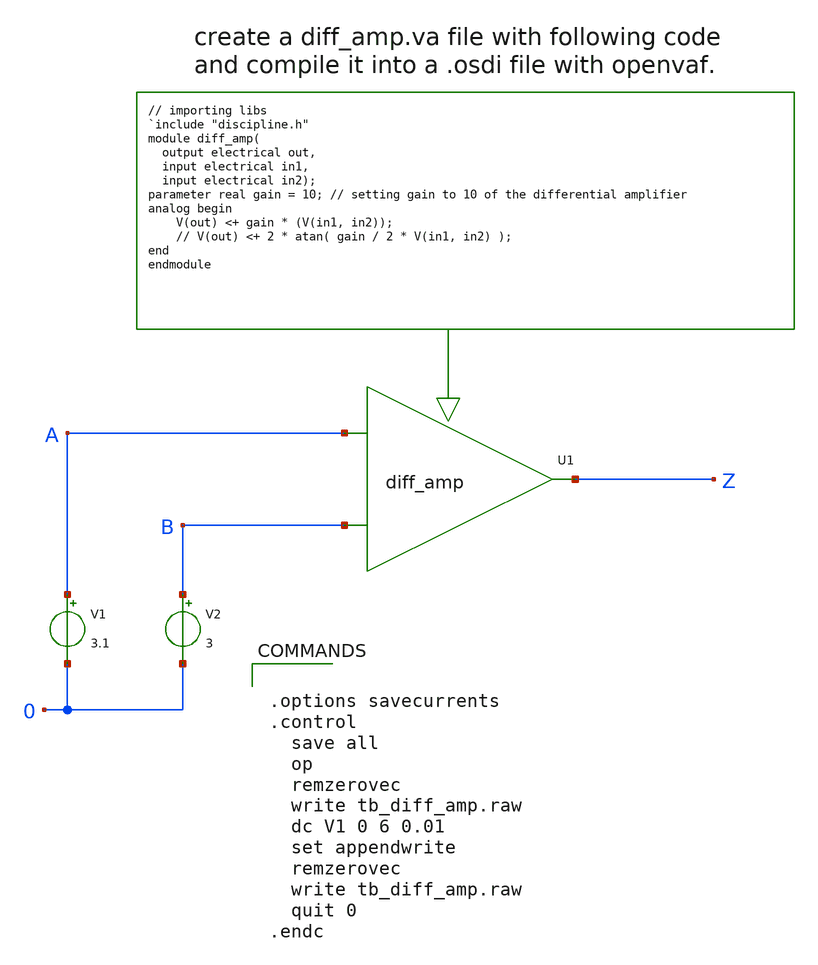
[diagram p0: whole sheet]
** sch_path: sky130A/xschem_libs/sky130_tests/tb_diff_amp/schematic/tb_diff_amp.sch
**.subckt tb_diff_amp
XU1 Z A B diff_amp_cell
V1 A 0 3.1
V2 B 0 3
**** begin user architecture code


.options savecurrents
.control
  save all
  op
  remzerovec
  write tb_diff_amp.raw
  dc V1 0 6 0.01
  set appendwrite
  remzerovec
  write tb_diff_amp.raw
  quit 0
.endc


**** end user architecture code
**.ends
**** begin user architecture code

.subckt diff_amp_cell OUT IN1 IN2
N1 out in1 in2 diff_amp_model
.ends diff_amp_cell

.model diff_amp_model diff_amp

.control
* following line specifies the location for the .osdi file so ngspice can use it.
pre_osdi $USER_CONF_DIR/xschem_library/diff_amp.osdi
.endc

**** end user architecture code
.end
